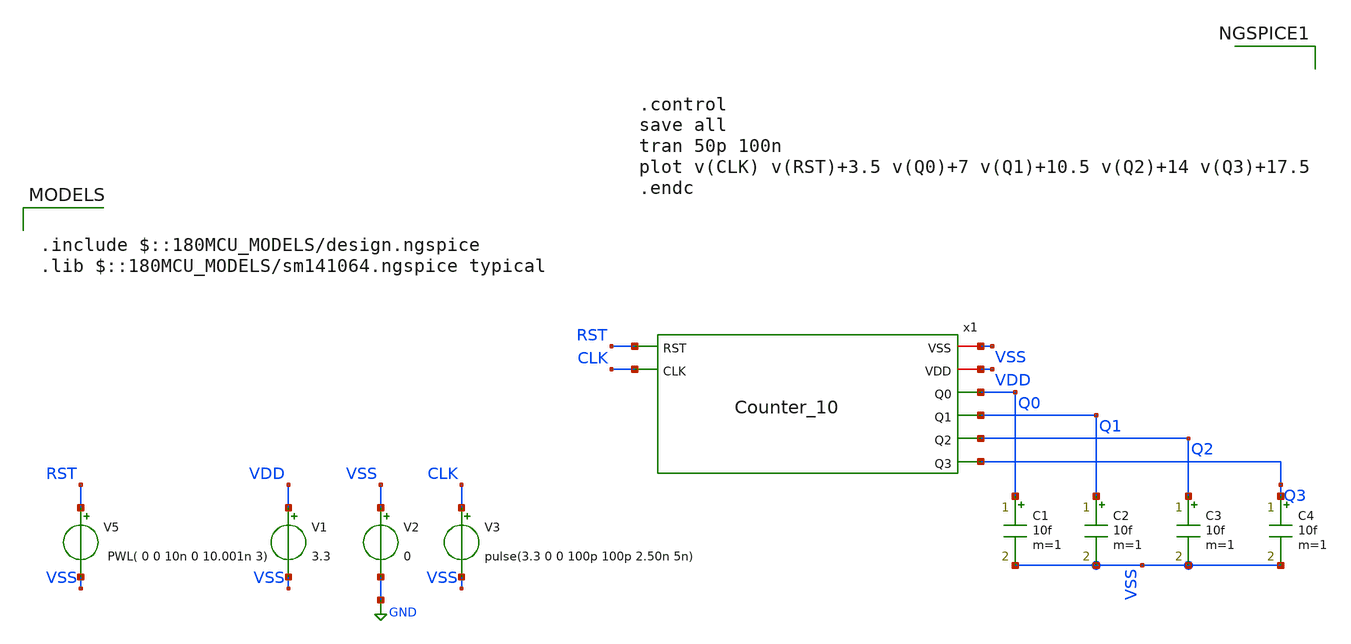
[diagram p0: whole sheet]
** sch_path: Clock_Generator_PAKISTAN_02/Schematics/Counter_10_TB.sch
**.subckt Counter_10_TB
V1 VDD VSS 3.3
V2 VSS GND 0
V3 CLK VSS pulse(3.3 0 0 100p 100p 2.50n 5n)
C1 Q0 VSS 10f m=1
C2 Q1 VSS 10f m=1
C3 Q2 VSS 10f m=1
C4 Q3 VSS 10f m=1
V5 RST VSS PWL( 0 0 10n 0 10.001n 3)
x1 VSS VDD Q0 Q1 RST Q2 Q3 CLK Counter_10
**** begin user architecture code

.include $::180MCU_MODELS/design.ngspice
.lib $::180MCU_MODELS/sm141064.ngspice typical




.control
save all
tran 50p 100n
plot v(CLK) v(RST)+3.5 v(Q0)+7 v(Q1)+10.5 v(Q2)+14 v(Q3)+17.5
.endc


**** end user architecture code
**.ends
.GLOBAL GND
.end
